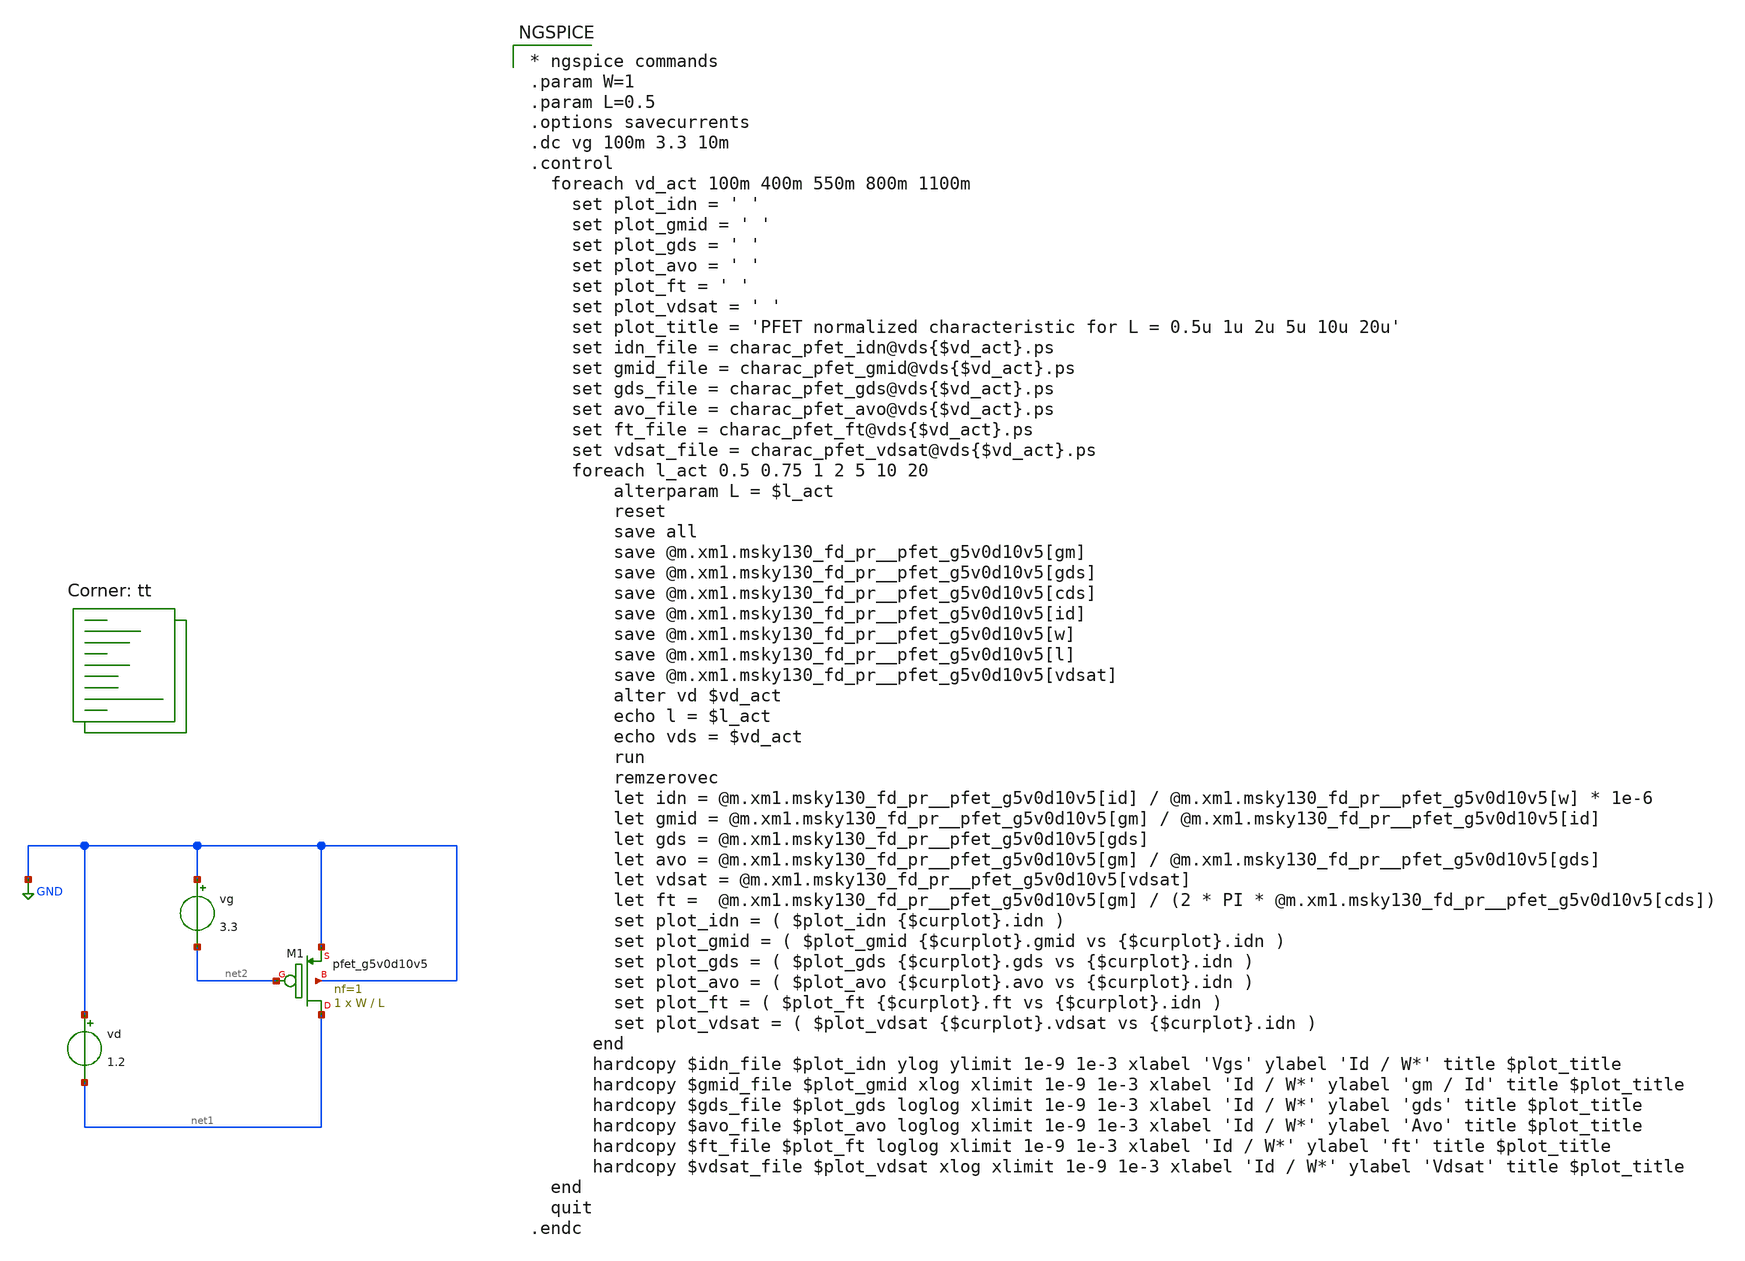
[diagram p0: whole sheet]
** sch_path: xschem/gmid_pfet_tb.sch
**.subckt gmid_pfet_tb
vd GND net1 1.2
vg GND net2 3.3
XM1 net1 net2 GND GND sky130_fd_pr__pfet_g5v0d10v5 L=L W=W nf=1 ad='int((nf+1)/2) * W/nf * 0.29' as='int((nf+2)/2) * W/nf * 0.29'
+ pd='2*int((nf+1)/2) * (W/nf + 0.29)' ps='2*int((nf+2)/2) * (W/nf + 0.29)' nrd='0.29 / W' nrs='0.29 / W'
+ sa=0 sb=0 sd=0 mult=1 m=1
**** begin user architecture code
.lib $::SKYWATER_MODELS/sky130.lib.spice tt

* ngspice commands
.param W=1
.param L=0.5
.options savecurrents
.dc vg 100m 3.3 10m
.control
  foreach vd_act 100m 400m 550m 800m 1100m
    set plot_idn = ' '
    set plot_gmid = ' '
    set plot_gds = ' '
    set plot_avo = ' '
    set plot_ft = ' '
    set plot_vdsat = ' '
    set plot_title = 'PFET normalized characteristic for L = 0.5u 1u 2u 5u 10u 20u'
    set idn_file = charac_pfet_idn@vds{$vd_act}.ps
    set gmid_file = charac_pfet_gmid@vds{$vd_act}.ps
    set gds_file = charac_pfet_gds@vds{$vd_act}.ps
    set avo_file = charac_pfet_avo@vds{$vd_act}.ps
    set ft_file = charac_pfet_ft@vds{$vd_act}.ps
    set vdsat_file = charac_pfet_vdsat@vds{$vd_act}.ps
    foreach l_act 0.5 0.75 1 2 5 10 20
        alterparam L = $l_act
        reset
        save all
        save @m.xm1.msky130_fd_pr__pfet_g5v0d10v5[gm]
        save @m.xm1.msky130_fd_pr__pfet_g5v0d10v5[gds]
        save @m.xm1.msky130_fd_pr__pfet_g5v0d10v5[cds]
        save @m.xm1.msky130_fd_pr__pfet_g5v0d10v5[id]
        save @m.xm1.msky130_fd_pr__pfet_g5v0d10v5[w]
        save @m.xm1.msky130_fd_pr__pfet_g5v0d10v5[l]
        save @m.xm1.msky130_fd_pr__pfet_g5v0d10v5[vdsat]
        alter vd $vd_act
        echo l = $l_act
        echo vds = $vd_act
        run
        remzerovec
        let idn = @m.xm1.msky130_fd_pr__pfet_g5v0d10v5[id] / @m.xm1.msky130_fd_pr__pfet_g5v0d10v5[w]
+ * 1e-6
        let gmid = @m.xm1.msky130_fd_pr__pfet_g5v0d10v5[gm] /
+ @m.xm1.msky130_fd_pr__pfet_g5v0d10v5[id]
        let gds = @m.xm1.msky130_fd_pr__pfet_g5v0d10v5[gds]
        let avo = @m.xm1.msky130_fd_pr__pfet_g5v0d10v5[gm] /
+ @m.xm1.msky130_fd_pr__pfet_g5v0d10v5[gds]
        let vdsat = @m.xm1.msky130_fd_pr__pfet_g5v0d10v5[vdsat]
        let ft =  @m.xm1.msky130_fd_pr__pfet_g5v0d10v5[gm] / (2 * PI *
+ @m.xm1.msky130_fd_pr__pfet_g5v0d10v5[cds])
        set plot_idn = ( $plot_idn {$curplot}.idn )
        set plot_gmid = ( $plot_gmid {$curplot}.gmid vs {$curplot}.idn )
        set plot_gds = ( $plot_gds {$curplot}.gds vs {$curplot}.idn )
        set plot_avo = ( $plot_avo {$curplot}.avo vs {$curplot}.idn )
        set plot_ft = ( $plot_ft {$curplot}.ft vs {$curplot}.idn )
        set plot_vdsat = ( $plot_vdsat {$curplot}.vdsat vs {$curplot}.idn )
      end
      hardcopy $idn_file $plot_idn ylog ylimit 1e-9 1e-3 xlabel 'Vgs' ylabel 'Id / W*' title $plot_title
      hardcopy $gmid_file $plot_gmid xlog xlimit 1e-9 1e-3 xlabel 'Id / W*' ylabel 'gm / Id' title $plot_title
      hardcopy $gds_file $plot_gds loglog xlimit 1e-9 1e-3 xlabel 'Id / W*' ylabel 'gds' title $plot_title
      hardcopy $avo_file $plot_avo loglog xlimit 1e-9 1e-3 xlabel 'Id / W*' ylabel 'Avo' title $plot_title
      hardcopy $ft_file $plot_ft loglog xlimit 1e-9 1e-3 xlabel 'Id / W*' ylabel 'ft' title $plot_title
      hardcopy $vdsat_file $plot_vdsat xlog xlimit 1e-9 1e-3 xlabel 'Id / W*' ylabel 'Vdsat' title $plot_title
  end
  quit
.endc


**** end user architecture code
**.ends
.GLOBAL GND
.end
